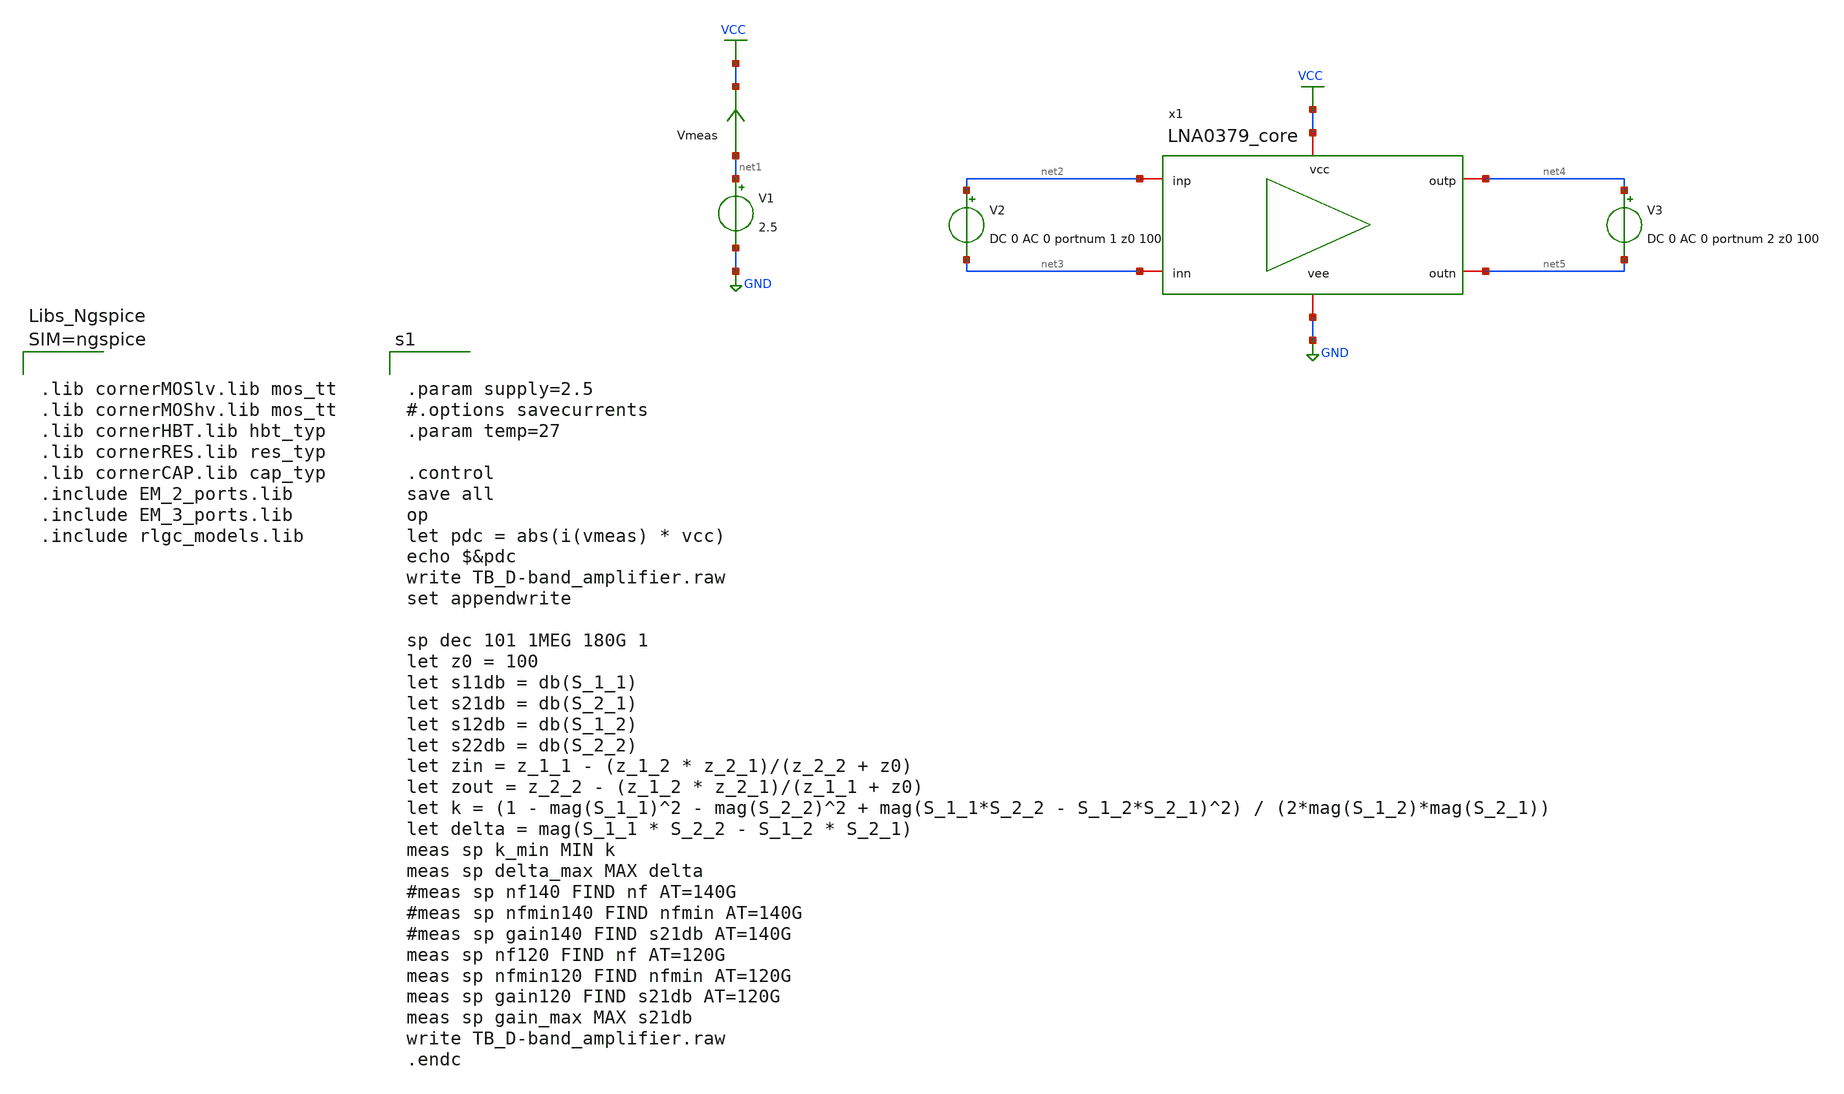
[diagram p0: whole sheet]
** sch_path: LNA0379-main/testbenches/ac/xschem/LNA0379_sp_tb.sch
**.subckt LNA0379_sp_tb
V1 net1 GND 2.5
V2 net2 net3 DC 0 AC 0 portnum 1 z0 100
V3 net4 net5 DC 0 AC 0 portnum 2 z0 100
Vmeas net1 VCC 0
.save i(vmeas)
x1 VCC net4 net5 net2 net3 GND LNA0379_core
**** begin user architecture code



.lib cornerMOSlv.lib mos_tt
.lib cornerMOShv.lib mos_tt
.lib cornerHBT.lib hbt_typ
.lib cornerRES.lib res_typ
.lib cornerCAP.lib cap_typ
.include EM_2_ports.lib
.include EM_3_ports.lib
.include rlgc_models.lib





.param supply=2.5
#.options savecurrents
.param temp=27

.control
save all
op
let pdc = abs(i(vmeas) * vcc)
echo $&pdc
write TB_D-band_amplifier.raw
set appendwrite

sp dec 101 1MEG 180G 1
let z0 = 100
let s11db = db(S_1_1)
let s21db = db(S_2_1)
let s12db = db(S_1_2)
let s22db = db(S_2_2)
let zin = z_1_1 - (z_1_2 * z_2_1)/(z_2_2 + z0)
let zout = z_2_2 - (z_1_2 * z_2_1)/(z_1_1 + z0)
let k = (1 - mag(S_1_1)^2 - mag(S_2_2)^2 + mag(S_1_1*S_2_2 - S_1_2*S_2_1)^2) /
+ (2*mag(S_1_2)*mag(S_2_1))
let delta = mag(S_1_1 * S_2_2 - S_1_2 * S_2_1)
meas sp k_min MIN k
meas sp delta_max MAX delta
#meas sp nf140 FIND nf AT=140G
#meas sp nfmin140 FIND nfmin AT=140G
#meas sp gain140 FIND s21db AT=140G
meas sp nf120 FIND nf AT=120G
meas sp nfmin120 FIND nfmin AT=120G
meas sp gain120 FIND s21db AT=120G
meas sp gain_max MAX s21db
write TB_D-band_amplifier.raw
.endc


**** end user architecture code
**.ends
.GLOBAL GND
.GLOBAL VCC
.end
